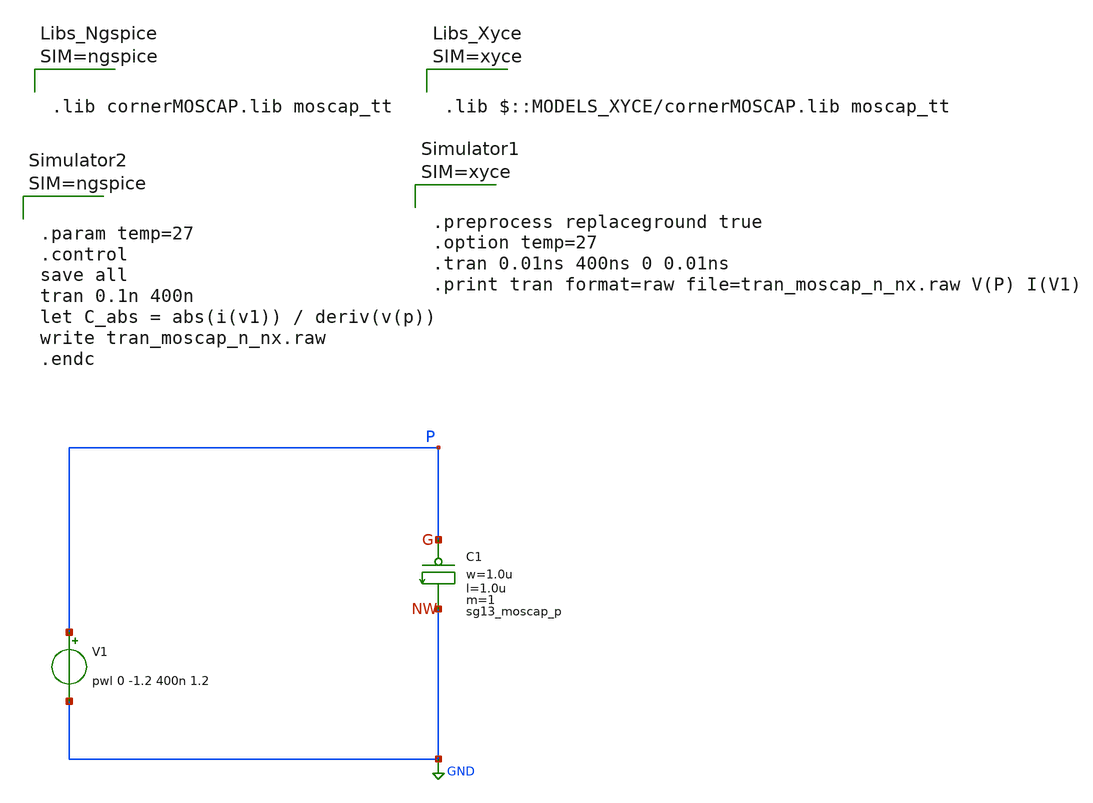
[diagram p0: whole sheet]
** sch_path: ihp-sg13g2/libs.tech/xschem/sg13g2_tests_xyce/tran_moscap_p.sch
**.subckt tran_moscap_p
V1 P GND pwl 0 -1.2 400n 1.2
XC1 P GND sg13_moscap_p w=1.0u l=1.0u m=1 mm_ok=1
**** begin user architecture code



.lib cornerMOSCAP.lib moscap_tt









.param temp=27
.control
save all
tran 0.1n 400n
let C_abs = abs(i(v1)) / deriv(v(p))
write tran_moscap_n_nx.raw
.endc






**** end user architecture code
**.ends
.GLOBAL GND
.end
